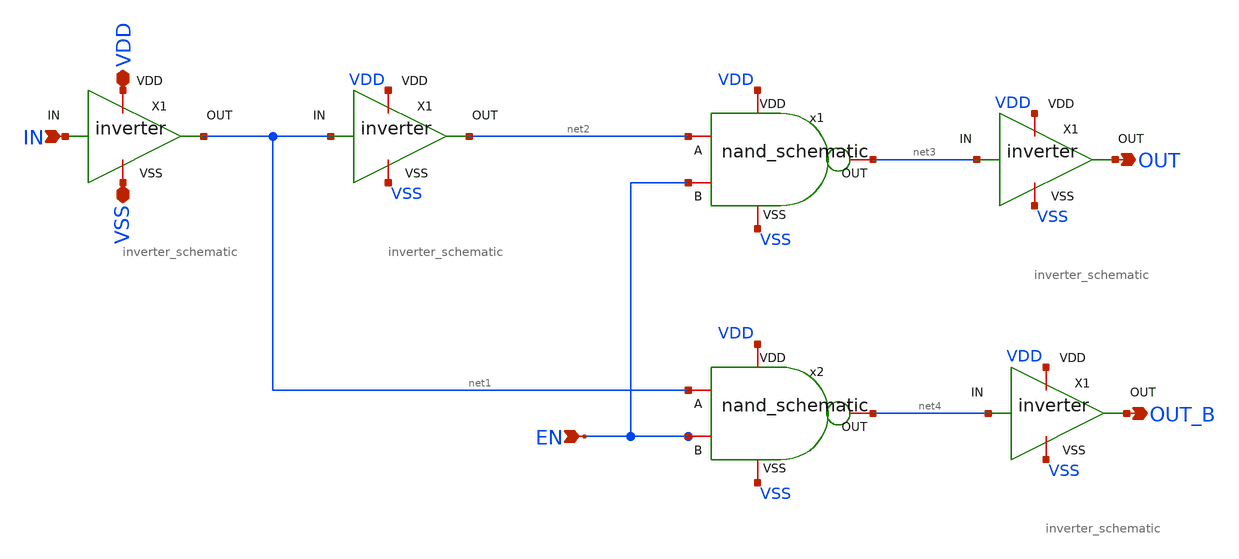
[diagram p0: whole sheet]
** sch_path: SRAM/row_decoder/schematic/row_decoder_schematic.sch
**.subckt row_decoder_schematic VDD VSS IN EN OUT OUT_B
*.iopin VDD
*.iopin VSS
*.ipin IN
*.ipin EN
*.opin OUT
*.opin OUT_B
x1 VDD net2 EN net3 VSS nand_schematic
x2 VDD net1 EN net4 VSS nand_schematic
x3 VDD net1 net2 VSS inverter_schematic
x4 VDD IN net1 VSS inverter_schematic
x5 VDD net3 OUT VSS inverter_schematic
x6 VDD net4 OUT_B VSS inverter_schematic
**.ends

* expanding   symbol:  nand_schematic.sym # of pins=5
** sym_path: SRAM/nand/schematic/nand_schematic.sym
** sch_path: SRAM/nand/schematic/nand_schematic.sch
.subckt nand_schematic VDD A B OUT VSS
*.iopin VDD
*.iopin VSS
*.iopin A
*.iopin B
*.iopin OUT
M1 OUT A VDD VDD pfet w=4.2u l=0.6u m=1
M2 OUT B VDD VDD pfet w=4.2u l=0.6u m=1
M3 OUT B net1 VSS nfet w=3.6u l=0.6u m=1
M4 net1 A VSS VSS nfet w=3.6u l=0.6u m=1
.ends


* expanding   symbol:  inverter_schematic.sym # of pins=4
** sym_path: SRAM/inverter/schematic/inverter_schematic.sym
** sch_path: SRAM/inverter/schematic/inverter_schematic.sch
.subckt inverter_schematic VDD IN OUT VSS
*.ipin IN
*.opin OUT
*.iopin VSS
*.iopin VDD
M2 OUT IN VSS VSS nfet w=1.8u l=0.6u m=1
M1 OUT IN VDD VDD pfet w=4.2u l=0.6u m=1
.ends

.end
